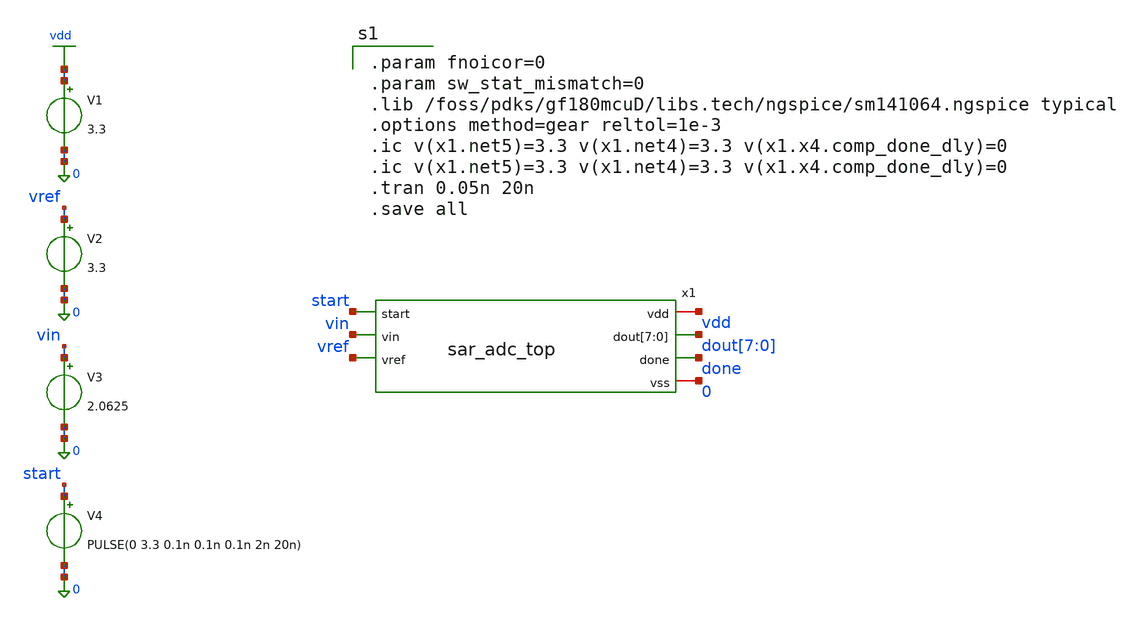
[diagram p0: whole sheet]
** sch_path: xschem/sar_adc/tb_sar_adc_top.sch
**.subckt tb_sar_adc_top
V1 vdd 0 3.3
V2 vref 0 3.3
V3 vin 0 2.0625
V4 start 0 PULSE(0 3.3 0.1n 0.1n 0.1n 2n 20n)
x1 vdd start vin dout[7] dout[6] dout[5] dout[4] dout[3] dout[2] dout[1] dout[0] done vref 0
+ sar_adc_top
**** begin user architecture code

.param fnoicor=0
.param sw_stat_mismatch=0
.lib /foss/pdks/gf180mcuD/libs.tech/ngspice/sm141064.ngspice typical
.options method=gear reltol=1e-3
.ic v(x1.net5)=3.3 v(x1.net4)=3.3 v(x1.x4.comp_done_dly)=0
.ic v(x1.net5)=3.3 v(x1.net4)=3.3 v(x1.x4.comp_done_dly)=0
.tran 0.05n 20n
.save all

**** end user architecture code
**.ends
.GLOBAL vdd
.end
